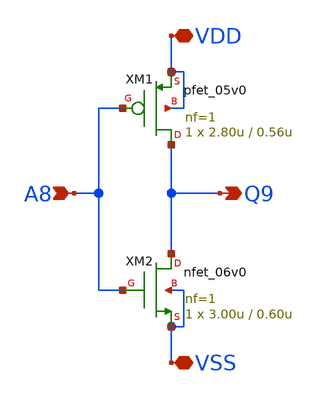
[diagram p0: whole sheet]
** sch_path: member_project/homelith/inverter/xschem/inv.sch
* Copyright 2022 GlobalFoundries PDK Authors
* Licensed under the Apache License, Version 2.0 (the "License");
* you may not use this file except in compliance with the License.
* You may obtain a copy of the License at
* https://www.apache.org/licenses/LICENSE-2.0
* Unless required by applicable law or agreed to in writing, software
* distributed under the License is distributed on an "AS IS" BASIS,
* WITHOUT WARRANTIES OR CONDITIONS OF ANY KIND, either express or implied.
* See the License for the specific language governing permissions and
* limitations under the License.
**.subckt inv A8 Q9 VDD VSS
*.ipin A8
*.opin Q9
*.iopin VDD
*.iopin VSS
XM1 Q9 A8 VDD VDD pfet_05v0 L=0.56u W=2.80u nf=1 ad='int((nf+1)/2) * W/nf * 0.18u' as='int((nf+2)/2) * W/nf * 0.18u'
+ pd='2*int((nf+1)/2) * (W/nf + 0.18u)' ps='2*int((nf+2)/2) * (W/nf + 0.18u)' nrd='0.18u / W' nrs='0.18u / W'
+ sa=0 sb=0 sd=0 m=1
XM2 Q9 A8 VSS VSS nfet_06v0 L=0.60u W=3.00u nf=1 ad='int((nf+1)/2) * W/nf * 0.18u' as='int((nf+2)/2) * W/nf * 0.18u'
+ pd='2*int((nf+1)/2) * (W/nf + 0.18u)' ps='2*int((nf+2)/2) * (W/nf + 0.18u)' nrd='0.18u / W' nrs='0.18u / W'
+ sa=0 sb=0 sd=0 m=1
**.ends
.end
